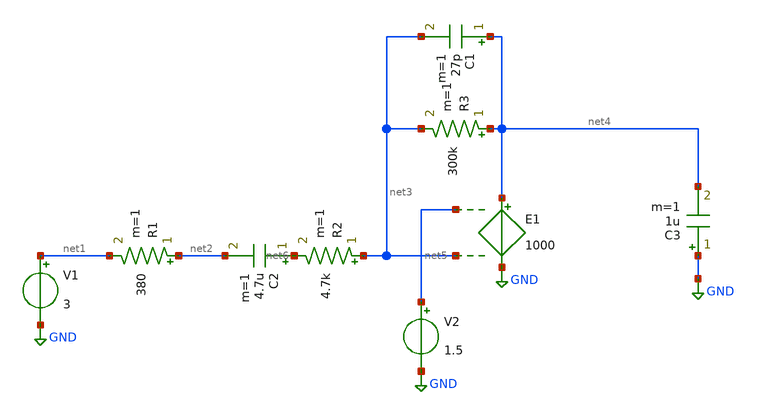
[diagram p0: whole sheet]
** sch_path: xschem/untitled.sch
**.subckt untitled
V1 net1 GND 3
R1 net2 net1 380 m=1
R2 net3 net6 4.7k m=1
C2 net6 net2 4.7u m=1
E1 net4 GND net5 net3 1000
R3 net4 net3 300k m=1
C1 net4 net3 27p m=1
C3 GND net4 1u m=1
V2 net5 GND 1.5
**.ends
.GLOBAL GND
.end
